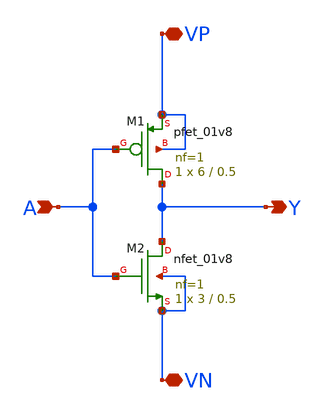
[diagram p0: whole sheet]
** sch_path: ADC/16bit_C2C/MagicAndSpice/EE431_FinalProj/inverterx3.sch
**.subckt inverterx3 A Y VP VN
*.ipin A
*.opin Y
*.iopin VP
*.iopin VN
XM1 Y A VP VP sky130_fd_pr__pfet_01v8 L=0.5 W=6 nf=1 ad='int((nf+1)/2) * W/nf * 0.29' as='int((nf+2)/2) * W/nf * 0.29'
+ pd='2*int((nf+1)/2) * (W/nf + 0.29)' ps='2*int((nf+2)/2) * (W/nf + 0.29)' nrd='0.29 / W' nrs='0.29 / W'
+ sa=0 sb=0 sd=0 mult=1 m=1
XM2 Y A VN VN sky130_fd_pr__nfet_01v8 L=0.5 W=3 nf=1 ad='int((nf+1)/2) * W/nf * 0.29' as='int((nf+2)/2) * W/nf * 0.29'
+ pd='2*int((nf+1)/2) * (W/nf + 0.29)' ps='2*int((nf+2)/2) * (W/nf + 0.29)' nrd='0.29 / W' nrs='0.29 / W'
+ sa=0 sb=0 sd=0 mult=1 m=1
**.ends
.end
